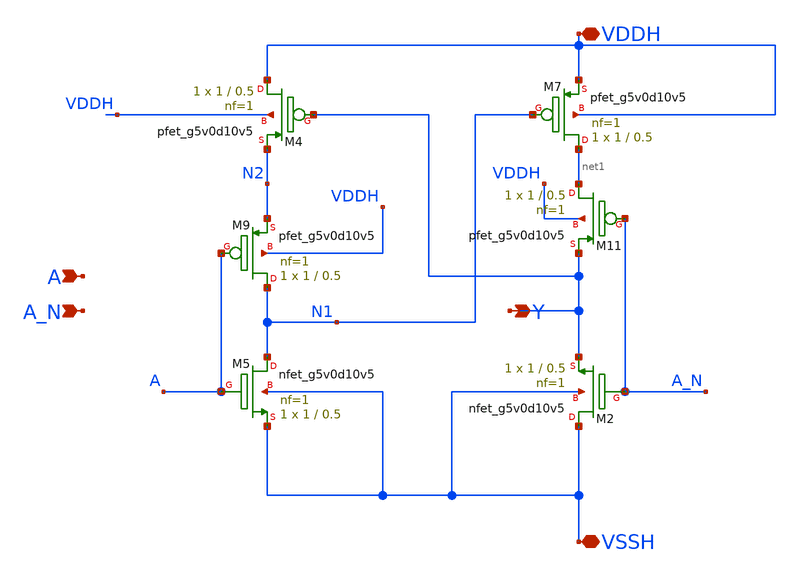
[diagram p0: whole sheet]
** sch_path: xschem/gpio/armleo_gpio_lv2hv.sch
**.subckt armleo_gpio_lv2hv A VDDH VSSH Y A_N
*.ipin A
*.iopin VDDH
*.iopin VSSH
*.opin Y
*.ipin A_N
XM2 VSSH A_N Y VSSH sky130_fd_pr__nfet_g5v0d10v5 L=0.5 W=1 nf=1 ad='int((nf+1)/2) * W/nf * 0.29' as='int((nf+2)/2) * W/nf * 0.29'
+ pd='2*int((nf+1)/2) * (W/nf + 0.29)' ps='2*int((nf+2)/2) * (W/nf + 0.29)' nrd='0.29 / W' nrs='0.29 / W'
+ sa=0 sb=0 sd=0 mult=1 m=1
XM5 N1 A VSSH VSSH sky130_fd_pr__nfet_g5v0d10v5 L=0.5 W=1 nf=1 ad='int((nf+1)/2) * W/nf * 0.29' as='int((nf+2)/2) * W/nf * 0.29'
+ pd='2*int((nf+1)/2) * (W/nf + 0.29)' ps='2*int((nf+2)/2) * (W/nf + 0.29)' nrd='0.29 / W' nrs='0.29 / W'
+ sa=0 sb=0 sd=0 mult=1 m=1
XM4 VDDH Y N2 VDDH sky130_fd_pr__pfet_g5v0d10v5 L=0.5 W=1 nf=1 ad='int((nf+1)/2) * W/nf * 0.29' as='int((nf+2)/2) * W/nf * 0.29'
+ pd='2*int((nf+1)/2) * (W/nf + 0.29)' ps='2*int((nf+2)/2) * (W/nf + 0.29)' nrd='0.29 / W' nrs='0.29 / W'
+ sa=0 sb=0 sd=0 mult=1 m=1
XM7 net1 N1 VDDH VDDH sky130_fd_pr__pfet_g5v0d10v5 L=0.5 W=1 nf=1 ad='int((nf+1)/2) * W/nf * 0.29' as='int((nf+2)/2) * W/nf * 0.29'
+ pd='2*int((nf+1)/2) * (W/nf + 0.29)' ps='2*int((nf+2)/2) * (W/nf + 0.29)' nrd='0.29 / W' nrs='0.29 / W'
+ sa=0 sb=0 sd=0 mult=1 m=1
XM9 N1 A N2 VDDH sky130_fd_pr__pfet_g5v0d10v5 L=0.5 W=1 nf=1 ad='int((nf+1)/2) * W/nf * 0.29' as='int((nf+2)/2) * W/nf * 0.29'
+ pd='2*int((nf+1)/2) * (W/nf + 0.29)' ps='2*int((nf+2)/2) * (W/nf + 0.29)' nrd='0.29 / W' nrs='0.29 / W'
+ sa=0 sb=0 sd=0 mult=1 m=1
XM11 net1 A_N Y VDDH sky130_fd_pr__pfet_g5v0d10v5 L=0.5 W=1 nf=1 ad='int((nf+1)/2) * W/nf * 0.29' as='int((nf+2)/2) * W/nf * 0.29'
+ pd='2*int((nf+1)/2) * (W/nf + 0.29)' ps='2*int((nf+2)/2) * (W/nf + 0.29)' nrd='0.29 / W' nrs='0.29 / W'
+ sa=0 sb=0 sd=0 mult=1 m=1
**.ends
.end
